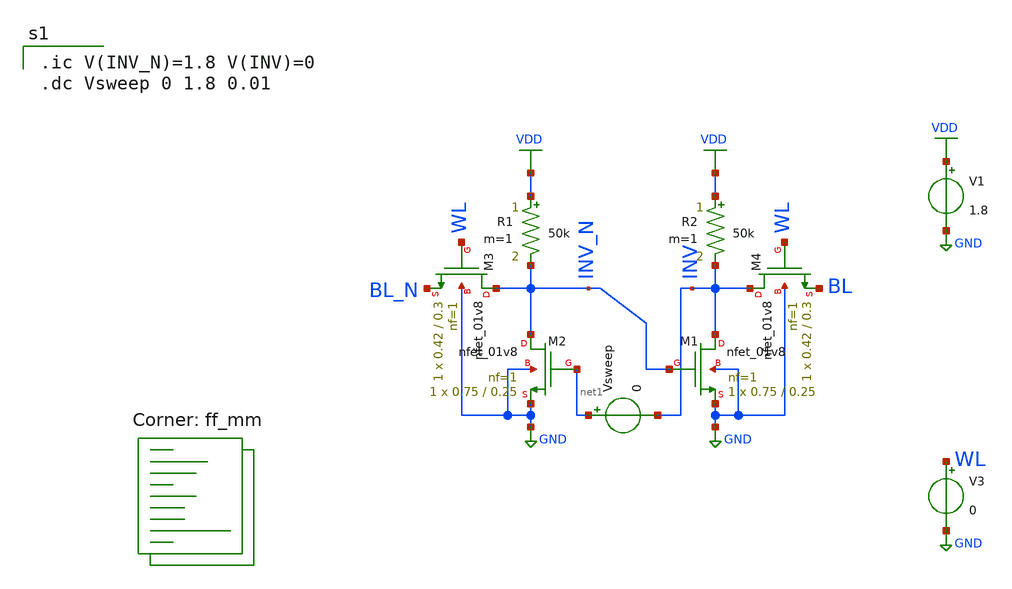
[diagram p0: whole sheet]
** sch_path: analog/schematics/sweep.sch
**.subckt sweep
XM1 INV INV_N GND GND sky130_fd_pr__nfet_01v8 L=0.25 W=0.75 nf=1 ad='int((nf+1)/2) * W/nf * 0.29' as='int((nf+2)/2) * W/nf * 0.29'
+ pd='2*int((nf+1)/2) * (W/nf + 0.29)' ps='2*int((nf+2)/2) * (W/nf + 0.29)' nrd='0.29 / W' nrs='0.29 / W'
+ sa=0 sb=0 sd=0 mult=1 m=1
R1 VDD INV_N 50k m=1
R2 VDD INV 50k m=1
XM3 INV_N WL BL_N GND sky130_fd_pr__nfet_01v8 L=0.3 W=0.42 nf=1 ad='int((nf+1)/2) * W/nf * 0.29' as='int((nf+2)/2) * W/nf * 0.29'
+ pd='2*int((nf+1)/2) * (W/nf + 0.29)' ps='2*int((nf+2)/2) * (W/nf + 0.29)' nrd='0.29 / W' nrs='0.29 / W'
+ sa=0 sb=0 sd=0 mult=1 m=1
XM4 INV WL BL GND sky130_fd_pr__nfet_01v8 L=0.3 W=0.42 nf=1 ad='int((nf+1)/2) * W/nf * 0.29' as='int((nf+2)/2) * W/nf * 0.29'
+ pd='2*int((nf+1)/2) * (W/nf + 0.29)' ps='2*int((nf+2)/2) * (W/nf + 0.29)' nrd='0.29 / W' nrs='0.29 / W'
+ sa=0 sb=0 sd=0 mult=1 m=1
XM2 INV_N net1 GND GND sky130_fd_pr__nfet_01v8 L=0.25 W=0.75 nf=1 ad='int((nf+1)/2) * W/nf * 0.29' as='int((nf+2)/2) * W/nf * 0.29'
+ pd='2*int((nf+1)/2) * (W/nf + 0.29)' ps='2*int((nf+2)/2) * (W/nf + 0.29)' nrd='0.29 / W' nrs='0.29 / W'
+ sa=0 sb=0 sd=0 mult=1 m=1
V1 VDD GND 1.8
V3 WL GND 0
Vsweep net1 INV 0
**** begin user architecture code

.ic V(INV_N)=1.8 V(INV)=0
.dc Vsweep 0 1.8 0.01

.lib $::SKYWATER_MODELS/sky130.lib.spice ff_mm
**** end user architecture code
**.ends
.GLOBAL VDD
.GLOBAL GND
.end
